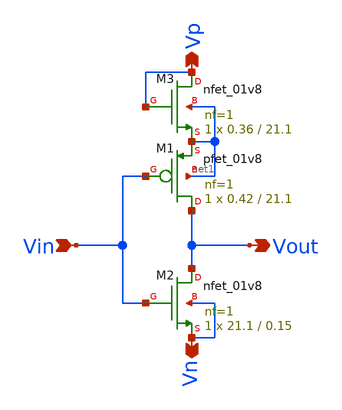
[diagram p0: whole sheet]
** sch_path: xschem/Vth_sch/Symbol/Inverter-th03.sch
**.subckt Inverter-th03 Vin Vout Vn Vp
*.ipin Vin
*.opin Vout
*.opin Vn
*.opin Vp
XM1 Vout Vin net1 net1 sky130_fd_pr__pfet_01v8 L=21.1 W=0.42 nf=1 ad='int((nf+1)/2) * W/nf * 0.29' as='int((nf+2)/2) * W/nf * 0.29'
+ pd='2*int((nf+1)/2) * (W/nf + 0.29)' ps='2*int((nf+2)/2) * (W/nf + 0.29)' nrd='0.29 / W' nrs='0.29 / W'
+ sa=0 sb=0 sd=0 mult=1 m=1
XM2 Vout Vin Vn Vn sky130_fd_pr__nfet_01v8 L=0.15 W=21.1 nf=1 ad='int((nf+1)/2) * W/nf * 0.29' as='int((nf+2)/2) * W/nf * 0.29'
+ pd='2*int((nf+1)/2) * (W/nf + 0.29)' ps='2*int((nf+2)/2) * (W/nf + 0.29)' nrd='0.29 / W' nrs='0.29 / W'
+ sa=0 sb=0 sd=0 mult=1 m=1
XM3 Vp Vp net1 net1 sky130_fd_pr__nfet_01v8 L=21.1 W=0.36 nf=1 ad='int((nf+1)/2) * W/nf * 0.29' as='int((nf+2)/2) * W/nf * 0.29'
+ pd='2*int((nf+1)/2) * (W/nf + 0.29)' ps='2*int((nf+2)/2) * (W/nf + 0.29)' nrd='0.29 / W' nrs='0.29 / W'
+ sa=0 sb=0 sd=0 mult=1 m=1
**.ends
.end
